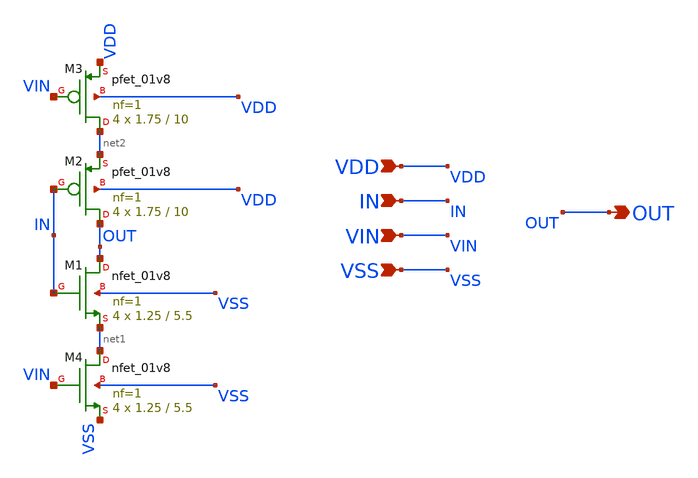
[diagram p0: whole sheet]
** sch_path: xschem/epc_delay.sch
**.subckt epc_delay VDD VIN IN VSS OUT
*.ipin VDD
*.ipin VIN
*.ipin IN
*.ipin VSS
*.opin OUT
XM1 OUT IN net1 VSS sky130_fd_pr__nfet_01v8 L=5.5 W=1.25 nf=1 ad='int((nf+1)/2) * W/nf * 0.29' as='int((nf+2)/2) * W/nf * 0.29'
+ pd='2*int((nf+1)/2) * (W/nf + 0.29)' ps='2*int((nf+2)/2) * (W/nf + 0.29)' nrd='0.29 / W' nrs='0.29 / W'
+ sa=0 sb=0 sd=0 mult=4 m=4
XM2 OUT IN net2 VDD sky130_fd_pr__pfet_01v8 L=10 W=1.75 nf=1 ad='int((nf+1)/2) * W/nf * 0.29' as='int((nf+2)/2) * W/nf * 0.29'
+ pd='2*int((nf+1)/2) * (W/nf + 0.29)' ps='2*int((nf+2)/2) * (W/nf + 0.29)' nrd='0.29 / W' nrs='0.29 / W'
+ sa=0 sb=0 sd=0 mult=4 m=4
XM3 net2 VIN VDD VDD sky130_fd_pr__pfet_01v8 L=10 W=1.75 nf=1 ad='int((nf+1)/2) * W/nf * 0.29' as='int((nf+2)/2) * W/nf * 0.29'
+ pd='2*int((nf+1)/2) * (W/nf + 0.29)' ps='2*int((nf+2)/2) * (W/nf + 0.29)' nrd='0.29 / W' nrs='0.29 / W'
+ sa=0 sb=0 sd=0 mult=4 m=4
XM4 net1 VIN VSS VSS sky130_fd_pr__nfet_01v8 L=5.5 W=1.25 nf=1 ad='int((nf+1)/2) * W/nf * 0.29' as='int((nf+2)/2) * W/nf * 0.29'
+ pd='2*int((nf+1)/2) * (W/nf + 0.29)' ps='2*int((nf+2)/2) * (W/nf + 0.29)' nrd='0.29 / W' nrs='0.29 / W'
+ sa=0 sb=0 sd=0 mult=4 m=4
**.ends
.end
